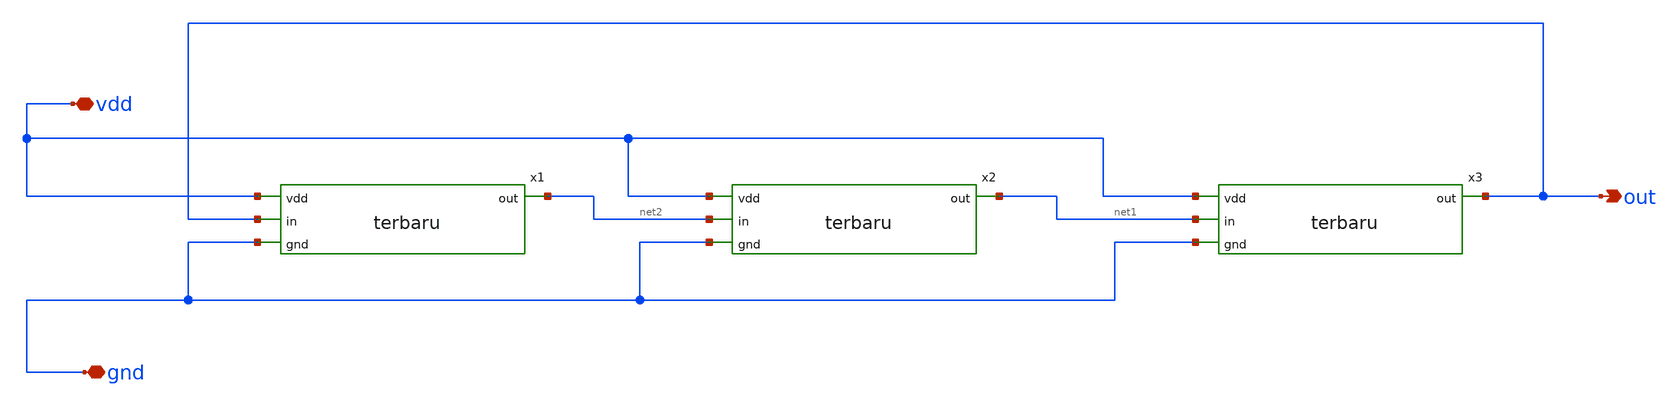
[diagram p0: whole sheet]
** sch_path: oscillator/oscillator/ringosibasic.sch
**.subckt ringosibasic vdd gnd out
*.iopin vdd
*.iopin gnd
*.opin out
x1 vdd out net2 gnd terbaru
x2 vdd net2 net1 gnd terbaru
x3 vdd net1 out gnd terbaru
**.ends

* expanding   symbol:  terbaru.sym # of pins=4
** sym_path: oscillator/oscillator/terbaru.sym
** sch_path: oscillator/oscillator/terbaru.sch
.subckt terbaru vdd in out gnd
*.ipin in
*.ipin gnd
*.ipin vdd
*.opin out
XM1 out in gnd gnd sky130_fd_pr__nfet_01v8 L=0.15 W=1 nf=1 ad='int((nf+1)/2) * W/nf * 0.29' as='int((nf+2)/2) * W/nf * 0.29'
+ pd='2*int((nf+1)/2) * (W/nf + 0.29)' ps='2*int((nf+2)/2) * (W/nf + 0.29)' nrd='0.29 / W' nrs='0.29 / W'
+ sa=0 sb=0 sd=0 mult=1 m=1
XM2 out in vdd vdd sky130_fd_pr__pfet_01v8 L=0.15 W=1 nf=1 ad='int((nf+1)/2) * W/nf * 0.29' as='int((nf+2)/2) * W/nf * 0.29'
+ pd='2*int((nf+1)/2) * (W/nf + 0.29)' ps='2*int((nf+2)/2) * (W/nf + 0.29)' nrd='0.29 / W' nrs='0.29 / W'
+ sa=0 sb=0 sd=0 mult=1 m=1
.ends

.end
